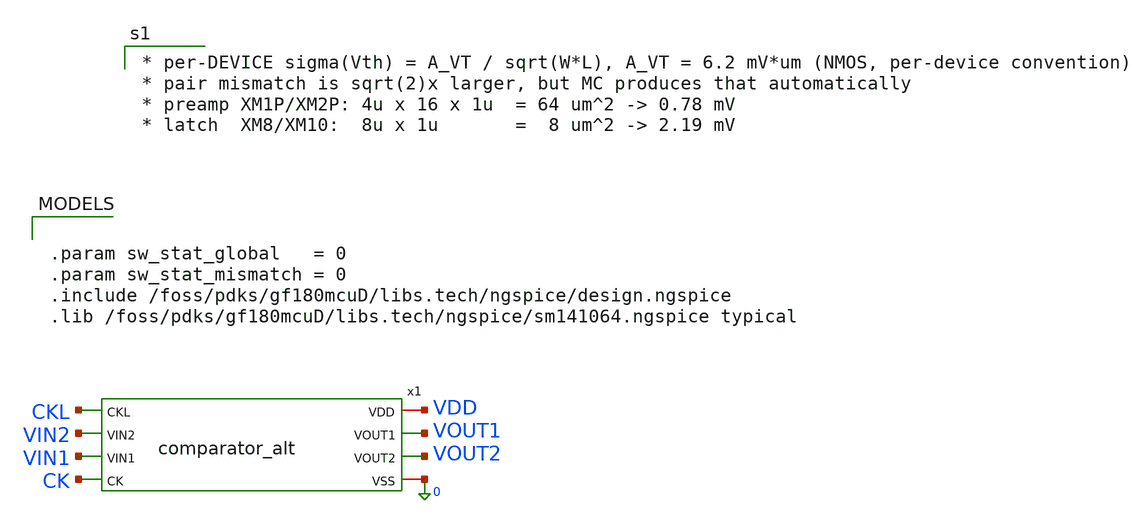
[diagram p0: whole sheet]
** sch_path: comparator_alt/schematic/tb_comparator_alt.sch
**.subckt tb_comparator_alt
x1 VDD CKL VIN2 VOUT1 VOUT2 VIN1 0 CK comparator_alt
**** begin user architecture code


.param sw_stat_global   = 0
.param sw_stat_mismatch = 0
.include /foss/pdks/gf180mcuD/libs.tech/ngspice/design.ngspice
.lib /foss/pdks/gf180mcuD/libs.tech/ngspice/sm141064.ngspice typical




* ===== stimulus =====
Vvdd  VDD  0 3.3
Vvin1 VIN1 0 PWL(0 1.64 1e-6 1.66)
Vvin2 VIN2 0 1.65
Vck   CK   0 PULSE(0 3.3 2n   100p 100p 8n 20n)
Vckl  CKL  0 PULSE(0 3.3 3.1n 100p 100p 5n 20n)

.control
let mc_runs = 200
let svt_pre = 0.78e-3
let svt_sa = 2.19e-3
let run = 0
set rndseed = 12345
let offset_results = vector(mc_runs)
let ngood = 0
let sumx = 0
let sumx2 = 0
set homeplot = $curplot
dowhile run < mc_runs
  echo ---- run $&run/$&mc_runs ----
  unset s_up
  unset s_dn
  alter @m.x1.x1.xm1p.m0[delvto] = svt_pre * sgauss(0)
  alter @m.x1.x1.xm2p.m0[delvto] = svt_pre * sgauss(0)
  alter @m.x1.x2.xm10.m0[delvto] = svt_sa  * sgauss(0)
  alter @m.x1.x2.xm8.m0[delvto]  = svt_sa  * sgauss(0)
  alter @vvin1[pwl] = [ 0 1.64 1e-6 1.66 ]
  tran 1n 1u
  let t_up = -1
  meas tran t_up when v(vout1)=1.5 fall=LAST
  if t_up > 0
    meas tran vin_up find v(vin1) at=t_up
    set s_up = $&vin_up
  end
  destroy $curplot
  alter @vvin1[pwl] = [ 0 1.66 1e-6 1.64 ]
  tran 1n 1u
  let t_dn = -1
  meas tran t_dn when v(vout1)=1.5 fall=1
  if t_dn > 0
    meas tran vin_dn find v(vin1) at=t_dn
    set s_dn = $&vin_dn
  end
  destroy $curplot
  setplot $homeplot
  if $?s_up * $?s_dn
    let cur = (($s_up - 1.65) + ($s_dn - 1.65)) / 2
    let offset_results[run] = cur
    let ngood = ngood + 1
    let sumx = sumx + cur
    let sumx2 = sumx2 + cur*cur
    echo   up=$s_up dn=$s_dn offset=$&cur
  else
    let offset_results[run] = -999
    echo   WARN: miss on run $&run
  end
  let run = run + 1
end
setplot $homeplot
let mu = sumx/ngood
let sig = sqrt(sumx2/ngood - mu*mu)
let mu_mv = mu*1e3
let sig_mv = sig*1e3
echo ==================================================
echo Two-stage offset MC:  N=$&mc_runs good=$&ngood
echo   mean = $&mu_mv mV   sigma = $&sig_mv mV
echo ==================================================

* --- save raw results to disk for later plotting ---
wrdata /foss/designs/comparator_alt/results/comp2_mc_offsets.txt offset_results
echo MC ckl=2.8n seed=12345 N=$&mc_runs good=$&ngood mean_mv=$&mu_mv sigma_mv=$&sig_mv >
+ /foss/designs/comparator_alt/results/comp2_mc_report.txt
print offset_results >> /foss/designs/comparator_alt/results/comp2_mc_report.txt
.endc




* SPICE component: <name> <node+> <node-> <value>
* V means voltage source, M is MOSFET, X is a subcircuit
* Node 0 is global ground
* PWL is a linear sweep from t=0, V=1.64, to t=1u, V=1.66, +/- 10 mV
* PULSE(v_low v_high initial_delay t_rise t_fall up_time period)
*
*
* Above .control is static netlist, below is simulation scripting
* let creates a vector (including length 1), set creates a shell var
* svt = sigma (standard deviation) of V threshold
* _pre = preamp input pair transistors, XM1P/XM2P
* _sa = strongarm input pair, XM8/XM10
* Random seed so that our results are reproducible exactly
* Create a vector with the number of slots equal to the number of runs
* Keep track of the sum of offsets and the sum of squares of offsets
* It lets us calculate variance later
*
* A new .tran opens a new plot, so keep track of the current plot
* Loop the following for each run of the Monte Carlo
* Print run number to terminal
* Clear s_up and s_dn so a failed run doesn't use last run's value
*
* alter changes an already-loaded variable. @=device instance parameter,
* m=MOSFET, x1.x1=preamp_dyn, m1p=transistor, m0=MOSFET inside nfet_03v3,
* [delvto]=parameter (delta v threshold), s_gauss(0)=random distribution
* centered on 0 with std. dev. 1, multiply by sigma to scale it right
* Start the up sweep of vin1 (Vvin1 denotes voltage of vin1)
* Transient simulation with 10ps steps ending at 1us
* Define t_up with a nonsense value so we know if it didn't change
* measure, let t_up=time when comparator flips (hits 1.5V)
* fall=LAST excludes the precharge to VDD; we want the most recent flip
* if there wasn't a flip, t_up would stay at -1 ^
* measure, let vin_up be the voltage at t_up that caused the flip ^
* save it in a shell variable so it doesn't get erased with the plot
* destroy the plot so we only have to remember our s_up voltage
* Do it again sweeping down to eliminate systematic bias
*
*
*
*
*
*
*
*
* Get back to the home plot where our variables are
* $?s_up asks if it exists (0 or 1), so this checks if both exist
* Calculate offset with average of up and down sweep offsets
* Add it to the vector of all the offsets
* Increase number of good runs, since we made it to this point
* Add to the sum of offsets and the sum of their squares
*
* Print the outputs for every run
*
* If we missed, set the value to -999 so it's clearly wrong
* Also give a warning of a miss in the terminal
*
* Increase run number
*
* Back to homeplot (a little bit of redundancy)
* mu is the mean
* sig calculates variance, mean of squares minus square of the mean
* and then take the square root of that number
* Convert to mV for readability
*
* echo to print results to terminal
*
*
*
*
* wrdata writes to a plain text file for plotting elsewhere
* Single bracket (>) creates a file, double (>>) appends



* per-DEVICE sigma(Vth) = A_VT / sqrt(W*L), A_VT = 6.2 mV*um (NMOS, per-device convention)
* pair mismatch is sqrt(2)x larger, but MC produces that automatically
* preamp XM1P/XM2P: 4u x 16 x 1u  = 64 um^2 -> 0.78 mV
* latch  XM8/XM10:  8u x 1u       =  8 um^2 -> 2.19 mV

**** end user architecture code
**.ends

* expanding   symbol:  comparator_alt/schematic/comparator_alt.sym # of pins=8
** sym_path: comparator_alt/schematic/comparator_alt.sym
** sch_path: comparator_alt/schematic/comparator_alt.sch
.subckt comparator_alt VDD CKL VIN2 VOUT1 VOUT2 VIN1 VSS CK
*.ipin CKL
*.ipin VIN2
*.ipin VIN1
*.ipin CK
*.opin VOUT2
*.opin VOUT1
*.iopin VDD
*.iopin VSS
x1 CKL VIN2 VDD VOUT1 VIN1 VOUT2 CK VSS comparator_2stage
**** begin user architecture code

*Outputs purposely crossed to match polarity with rest of ADC

**** end user architecture code
.ends


* expanding   symbol:  comparator_alt/schematic/comparator_2stage.sym # of pins=8
** sym_path: comparator/schematic/comparator_2stage.sym
** sch_path: comparator/schematic/comparator_2stage.sch
.subckt comparator_2stage CKL VIN2 VDD VOUT2 VIN1 VOUT1 CK VSS
*.ipin CK
*.iopin VDD
*.iopin VSS
*.ipin VIN1
*.ipin VIN2
*.opin VOUT2
*.opin VOUT1
*.ipin CKL
x2 VDD DIP1 DIP2 VIN2 VIN1 CK VSS preamp_dyn
x4 VDD CKL VOUT2 VOUT1 DIP2 DIP1 VSS strongarm_2
.ends


* expanding   symbol:  comparator/schematic/preamp_dyn.sym # of pins=7
** sym_path: comparator_alt/schematic/preamp_dyn.sym
** sch_path: comparator_alt/schematic/preamp_dyn.sch
.subckt preamp_dyn VDD DIP2 DIP1 VIN2 VIN1 CK VSS
*.ipin VIN1
*.ipin VIN2
*.iopin VDD
*.iopin VSS
*.opin DIP1
*.opin DIP2
*.ipin CK
XM1P DIP1 VIN1 TAIL VSS nfet_03v3 L=1u W=4u nf=1 ad='int((nf+1)/2) * W/nf * 0.18u' as='int((nf+2)/2) * W/nf * 0.18u'
+ pd='2*int((nf+1)/2) * (W/nf + 0.18u)' ps='2*int((nf+2)/2) * (W/nf + 0.18u)' nrd='0.18u / W' nrs='0.18u / W'
+ sa=0 sb=0 sd=0 m=16
XMT1 TAIL CK VSS VSS nfet_03v3 L=1u W=1u nf=1 ad='int((nf+1)/2) * W/nf * 0.18u' as='int((nf+2)/2) * W/nf * 0.18u'
+ pd='2*int((nf+1)/2) * (W/nf + 0.18u)' ps='2*int((nf+2)/2) * (W/nf + 0.18u)' nrd='0.18u / W' nrs='0.18u / W'
+ sa=0 sb=0 sd=0 m=1
XM2P DIP2 VIN2 TAIL VSS nfet_03v3 L=1u W=4u nf=1 ad='int((nf+1)/2) * W/nf * 0.18u' as='int((nf+2)/2) * W/nf * 0.18u'
+ pd='2*int((nf+1)/2) * (W/nf + 0.18u)' ps='2*int((nf+2)/2) * (W/nf + 0.18u)' nrd='0.18u / W' nrs='0.18u / W'
+ sa=0 sb=0 sd=0 m=16
XMP1 DIP1 CK VDD VDD pfet_03v3 L=0.3u W=3u nf=1 ad='int((nf+1)/2) * W/nf * 0.18u' as='int((nf+2)/2) * W/nf * 0.18u'
+ pd='2*int((nf+1)/2) * (W/nf + 0.18u)' ps='2*int((nf+2)/2) * (W/nf + 0.18u)' nrd='0.18u / W' nrs='0.18u / W'
+ sa=0 sb=0 sd=0 m=1
XMP2 DIP2 CK VDD VDD pfet_03v3 L=0.3u W=3u nf=1 ad='int((nf+1)/2) * W/nf * 0.18u' as='int((nf+2)/2) * W/nf * 0.18u'
+ pd='2*int((nf+1)/2) * (W/nf + 0.18u)' ps='2*int((nf+2)/2) * (W/nf + 0.18u)' nrd='0.18u / W' nrs='0.18u / W'
+ sa=0 sb=0 sd=0 m=1
.ends


* expanding   symbol:  comparator/schematic/strongarm_2.sym # of pins=7
** sym_path: comparator_alt/schematic/strongarm_2.sym
** sch_path: comparator_alt/schematic/strongarm_2.sch
.subckt strongarm_2 VDD CK VOUT2 VOUT1 VIN1 VIN2 VSS
*.opin VOUT1
*.opin VOUT2
*.ipin VIN1
*.ipin VIN2
*.ipin CK
*.iopin VDD
*.iopin VSS
XM1 VOUT2 VOUT1 net1 VSS nfet_03v3 L=0.28u W=2u nf=1 ad='int((nf+1)/2) * W/nf * 0.18u' as='int((nf+2)/2) * W/nf * 0.18u'
+ pd='2*int((nf+1)/2) * (W/nf + 0.18u)' ps='2*int((nf+2)/2) * (W/nf + 0.18u)' nrd='0.18u / W' nrs='0.18u / W'
+ sa=0 sb=0 sd=0 m=1
XM2 VOUT1 VOUT2 VDD VDD pfet_03v3 L=0.28u W=0.42u nf=1 ad='int((nf+1)/2) * W/nf * 0.18u' as='int((nf+2)/2) * W/nf * 0.18u'
+ pd='2*int((nf+1)/2) * (W/nf + 0.18u)' ps='2*int((nf+2)/2) * (W/nf + 0.18u)' nrd='0.18u / W' nrs='0.18u / W'
+ sa=0 sb=0 sd=0 m=1
XM3 VOUT1 CK VDD VDD pfet_03v3 L=0.28u W=5u nf=1 ad='int((nf+1)/2) * W/nf * 0.18u' as='int((nf+2)/2) * W/nf * 0.18u'
+ pd='2*int((nf+1)/2) * (W/nf + 0.18u)' ps='2*int((nf+2)/2) * (W/nf + 0.18u)' nrd='0.18u / W' nrs='0.18u / W'
+ sa=0 sb=0 sd=0 m=1
XM4 net3 CK VDD VDD pfet_03v3 L=0.28u W=5u nf=1 ad='int((nf+1)/2) * W/nf * 0.18u' as='int((nf+2)/2) * W/nf * 0.18u'
+ pd='2*int((nf+1)/2) * (W/nf + 0.18u)' ps='2*int((nf+2)/2) * (W/nf + 0.18u)' nrd='0.18u / W' nrs='0.18u / W'
+ sa=0 sb=0 sd=0 m=1
XM5 net1 CK VDD VDD pfet_03v3 L=0.28u W=5u nf=1 ad='int((nf+1)/2) * W/nf * 0.18u' as='int((nf+2)/2) * W/nf * 0.18u'
+ pd='2*int((nf+1)/2) * (W/nf + 0.18u)' ps='2*int((nf+2)/2) * (W/nf + 0.18u)' nrd='0.18u / W' nrs='0.18u / W'
+ sa=0 sb=0 sd=0 m=1
XM6 VOUT2 CK VDD VDD pfet_03v3 L=0.28u W=5u nf=1 ad='int((nf+1)/2) * W/nf * 0.18u' as='int((nf+2)/2) * W/nf * 0.18u'
+ pd='2*int((nf+1)/2) * (W/nf + 0.18u)' ps='2*int((nf+2)/2) * (W/nf + 0.18u)' nrd='0.18u / W' nrs='0.18u / W'
+ sa=0 sb=0 sd=0 m=1
XM7 VOUT2 VOUT1 VDD VDD pfet_03v3 L=0.28u W=0.42u nf=1 ad='int((nf+1)/2) * W/nf * 0.18u' as='int((nf+2)/2) * W/nf * 0.18u'
+ pd='2*int((nf+1)/2) * (W/nf + 0.18u)' ps='2*int((nf+2)/2) * (W/nf + 0.18u)' nrd='0.18u / W' nrs='0.18u / W'
+ sa=0 sb=0 sd=0 m=1
XM8 net1 VIN2 net2 VSS nfet_03v3 L=1u W=8u nf=1 ad='int((nf+1)/2) * W/nf * 0.18u' as='int((nf+2)/2) * W/nf * 0.18u'
+ pd='2*int((nf+1)/2) * (W/nf + 0.18u)' ps='2*int((nf+2)/2) * (W/nf + 0.18u)' nrd='0.18u / W' nrs='0.18u / W'
+ sa=0 sb=0 sd=0 m=1
XM9 VOUT1 VOUT2 net3 VSS nfet_03v3 L=0.28u W=2u nf=1 ad='int((nf+1)/2) * W/nf * 0.18u' as='int((nf+2)/2) * W/nf * 0.18u'
+ pd='2*int((nf+1)/2) * (W/nf + 0.18u)' ps='2*int((nf+2)/2) * (W/nf + 0.18u)' nrd='0.18u / W' nrs='0.18u / W'
+ sa=0 sb=0 sd=0 m=1
XM10 net3 VIN1 net2 VSS nfet_03v3 L=1u W=8u nf=1 ad='int((nf+1)/2) * W/nf * 0.18u' as='int((nf+2)/2) * W/nf * 0.18u'
+ pd='2*int((nf+1)/2) * (W/nf + 0.18u)' ps='2*int((nf+2)/2) * (W/nf + 0.18u)' nrd='0.18u / W' nrs='0.18u / W'
+ sa=0 sb=0 sd=0 m=1
XM11 net2 CK VSS VSS nfet_03v3 L=0.28u W=2u nf=1 ad='int((nf+1)/2) * W/nf * 0.18u' as='int((nf+2)/2) * W/nf * 0.18u'
+ pd='2*int((nf+1)/2) * (W/nf + 0.18u)' ps='2*int((nf+2)/2) * (W/nf + 0.18u)' nrd='0.18u / W' nrs='0.18u / W'
+ sa=0 sb=0 sd=0 m=1
.ends

.end
